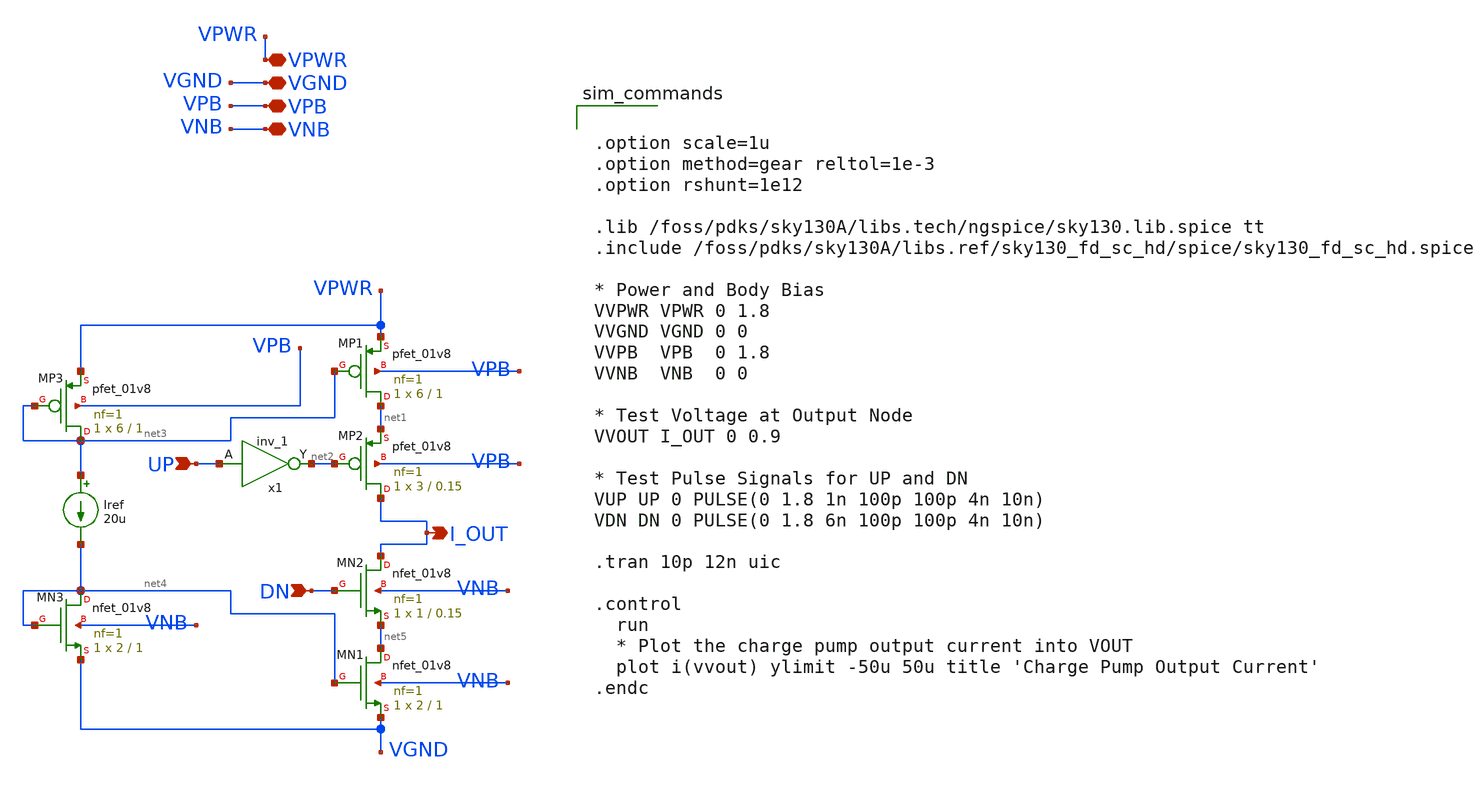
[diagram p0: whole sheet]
** sch_path: cp_tb.sch
**.subckt cp_tb UP DN VPWR VGND VPB VNB I_OUT
*.ipin UP
*.ipin DN
*.iopin VPWR
*.iopin VGND
*.iopin VPB
*.iopin VNB
*.opin I_OUT
XMN1 net5 net4 VGND VNB sky130_fd_pr__nfet_01v8 L=1 W=2 nf=1 ad='int((1 + 1)/2) * 2 / 1 * 0.29' as='int((1 + 2)/2) * 2 / 1 * 0.29'
+ pd='2*int((1 + 1)/2) * (2 / 1 + 0.29)' ps='2*int((1 + 2)/2) * (2 / 1 + 0.29)' nrd='0.29 / 2 ' nrs='0.29 / 2 '
+ sa=0 sb=0 sd=0 mult=1 m=1
XMP1 net1 net3 VPWR VPB sky130_fd_pr__pfet_01v8 L=1 W=6 nf=1 ad='int((1 + 1)/2) * 6 / 1 * 0.29' as='int((1 + 2)/2) * 6 / 1 * 0.29'
+ pd='2*int((1 + 1)/2) * (6 / 1 + 0.29)' ps='2*int((1 + 2)/2) * (6 / 1 + 0.29)' nrd='0.29 / 6 ' nrs='0.29 / 6 '
+ sa=0 sb=0 sd=0 mult=1 m=1
Iref net3 net4 20u
XMN2 I_OUT DN net5 VNB sky130_fd_pr__nfet_01v8 L=0.15 W=1 nf=1 ad='int((1 + 1)/2) * 1 / 1 * 0.29' as='int((1 + 2)/2) * 1 / 1 * 0.29'
+ pd='2*int((1 + 1)/2) * (1 / 1 + 0.29)' ps='2*int((1 + 2)/2) * (1 / 1 + 0.29)' nrd='0.29 / 1 ' nrs='0.29 / 1 '
+ sa=0 sb=0 sd=0 mult=1 m=1
XMP2 I_OUT net2 net1 VPB sky130_fd_pr__pfet_01v8 L=0.15 W=3 nf=1 ad='int((1 + 1)/2) * 3 / 1 * 0.29' as='int((1 + 2)/2) * 3 / 1 * 0.29'
+ pd='2*int((1 + 1)/2) * (3 / 1 + 0.29)' ps='2*int((1 + 2)/2) * (3 / 1 + 0.29)' nrd='0.29 / 3 ' nrs='0.29 / 3 '
+ sa=0 sb=0 sd=0 mult=1 m=1
x1 UP VGND VNB VPB VPWR net2 sky130_fd_sc_hd__inv_1
XMP3 net3 net3 VPWR VPB sky130_fd_pr__pfet_01v8 L=1 W=6 nf=1 ad='int((1 + 1)/2) * 6 / 1 * 0.29' as='int((1 + 2)/2) * 6 / 1 * 0.29'
+ pd='2*int((1 + 1)/2) * (6 / 1 + 0.29)' ps='2*int((1 + 2)/2) * (6 / 1 + 0.29)' nrd='0.29 / 6 ' nrs='0.29 / 6 '
+ sa=0 sb=0 sd=0 mult=1 m=1
XMN3 net4 net4 VGND VNB sky130_fd_pr__nfet_01v8 L=1 W=2 nf=1 ad='int((1 + 1)/2) * 2 / 1 * 0.29' as='int((1 + 2)/2) * 2 / 1 * 0.29'
+ pd='2*int((1 + 1)/2) * (2 / 1 + 0.29)' ps='2*int((1 + 2)/2) * (2 / 1 + 0.29)' nrd='0.29 / 2 ' nrs='0.29 / 2 '
+ sa=0 sb=0 sd=0 mult=1 m=1
**** begin user architecture code


.option scale=1u
.option method=gear reltol=1e-3
.option rshunt=1e12

.lib /foss/pdks/sky130A/libs.tech/ngspice/sky130.lib.spice tt
.include /foss/pdks/sky130A/libs.ref/sky130_fd_sc_hd/spice/sky130_fd_sc_hd.spice

* Power and Body Bias
VVPWR VPWR 0 1.8
VVGND VGND 0 0
VVPB  VPB  0 1.8
VVNB  VNB  0 0

* Test Voltage at Output Node
VVOUT I_OUT 0 0.9

* Test Pulse Signals for UP and DN
VUP UP 0 PULSE(0 1.8 1n 100p 100p 4n 10n)
VDN DN 0 PULSE(0 1.8 6n 100p 100p 4n 10n)

.tran 10p 12n uic

.control
  run
  * Plot the charge pump output current into VOUT
  plot i(vvout) ylimit -50u 50u title 'Charge Pump Output Current'
.endc


**** end user architecture code
**.ends
.end
